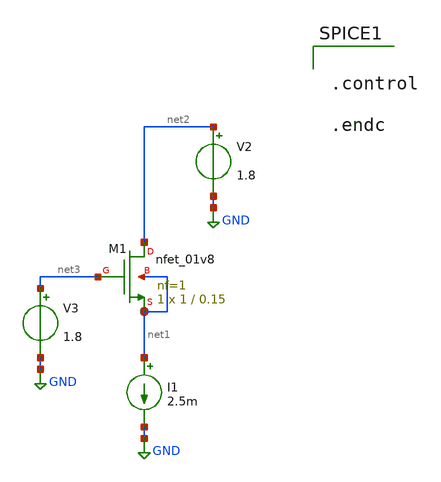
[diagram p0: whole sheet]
** sch_path: mos_sizing/nmos_gm_fix.sch
**.subckt nmos_gm_fix
XM1 net2 net3 net1 net1 sky130_fd_pr__nfet_01v8 L=0.15 W=1 nf=1 ad='int((nf+1)/2) * W/nf * 0.29' as='int((nf+2)/2) * W/nf * 0.29'
+ pd='2*int((nf+1)/2) * (W/nf + 0.29)' ps='2*int((nf+2)/2) * (W/nf + 0.29)' nrd='0.29 / W' nrs='0.29 / W'
+ sa=0 sb=0 sd=0 mult=1 m=1
I1 net1 GND 2.5m
V2 net2 GND 1.8
V3 net3 GND 1.8
**** begin user architecture code


.option wnflag = 1
.lib /usr/local/share/pdk/sky130A/libs.tech/ngspice/sky130.lib.spice tt
.include /usr/local/share/pdk/sky130A/libs.ref/sky130_fd_pr/spice/sky130_fd_pr__ind_05_220.model.spice
.param mc_mm_switch=0




.control

.endc


**** end user architecture code
**.ends
.GLOBAL GND
.end
